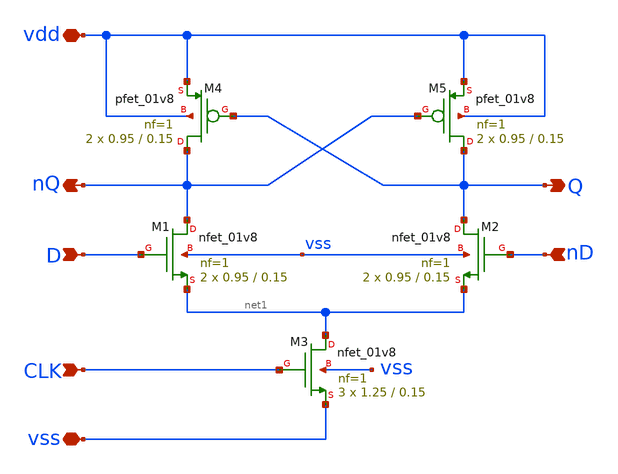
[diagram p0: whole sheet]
** sch_path: xschem/latch_diff.sch
**.subckt latch_diff vdd vss D nQ CLK nD Q
*.iopin vdd
*.iopin vss
*.ipin D
*.opin nQ
*.ipin CLK
*.ipin nD
*.opin Q
XM3 net1 CLK vss vss sky130_fd_pr__nfet_01v8 L=0.15 W=1.25 nf=1 ad='int((nf+1)/2) * W/nf * 0.29' as='int((nf+2)/2) * W/nf * 0.29'
+ pd='2*int((nf+1)/2) * (W/nf + 0.29)' ps='2*int((nf+2)/2) * (W/nf + 0.29)' nrd='0.29 / W' nrs='0.29 / W'
+ sa=0 sb=0 sd=0 mult=3 m=3
XM4 nQ Q vdd vdd sky130_fd_pr__pfet_01v8 L=0.15 W=0.95 nf=1 ad='int((nf+1)/2) * W/nf * 0.29' as='int((nf+2)/2) * W/nf * 0.29'
+ pd='2*int((nf+1)/2) * (W/nf + 0.29)' ps='2*int((nf+2)/2) * (W/nf + 0.29)' nrd='0.29 / W' nrs='0.29 / W'
+ sa=0 sb=0 sd=0 mult=2 m=2
XM5 Q nQ vdd vdd sky130_fd_pr__pfet_01v8 L=0.15 W=0.95 nf=1 ad='int((nf+1)/2) * W/nf * 0.29' as='int((nf+2)/2) * W/nf * 0.29'
+ pd='2*int((nf+1)/2) * (W/nf + 0.29)' ps='2*int((nf+2)/2) * (W/nf + 0.29)' nrd='0.29 / W' nrs='0.29 / W'
+ sa=0 sb=0 sd=0 mult=2 m=2
XM1 nQ D net1 vss sky130_fd_pr__nfet_01v8 L=0.15 W=0.95 nf=1 ad='int((nf+1)/2) * W/nf * 0.29' as='int((nf+2)/2) * W/nf * 0.29'
+ pd='2*int((nf+1)/2) * (W/nf + 0.29)' ps='2*int((nf+2)/2) * (W/nf + 0.29)' nrd='0.29 / W' nrs='0.29 / W'
+ sa=0 sb=0 sd=0 mult=2 m=2
XM2 Q nD net1 vss sky130_fd_pr__nfet_01v8 L=0.15 W=0.95 nf=1 ad='int((nf+1)/2) * W/nf * 0.29' as='int((nf+2)/2) * W/nf * 0.29'
+ pd='2*int((nf+1)/2) * (W/nf + 0.29)' ps='2*int((nf+2)/2) * (W/nf + 0.29)' nrd='0.29 / W' nrs='0.29 / W'
+ sa=0 sb=0 sd=0 mult=2 m=2
**.ends
.end
